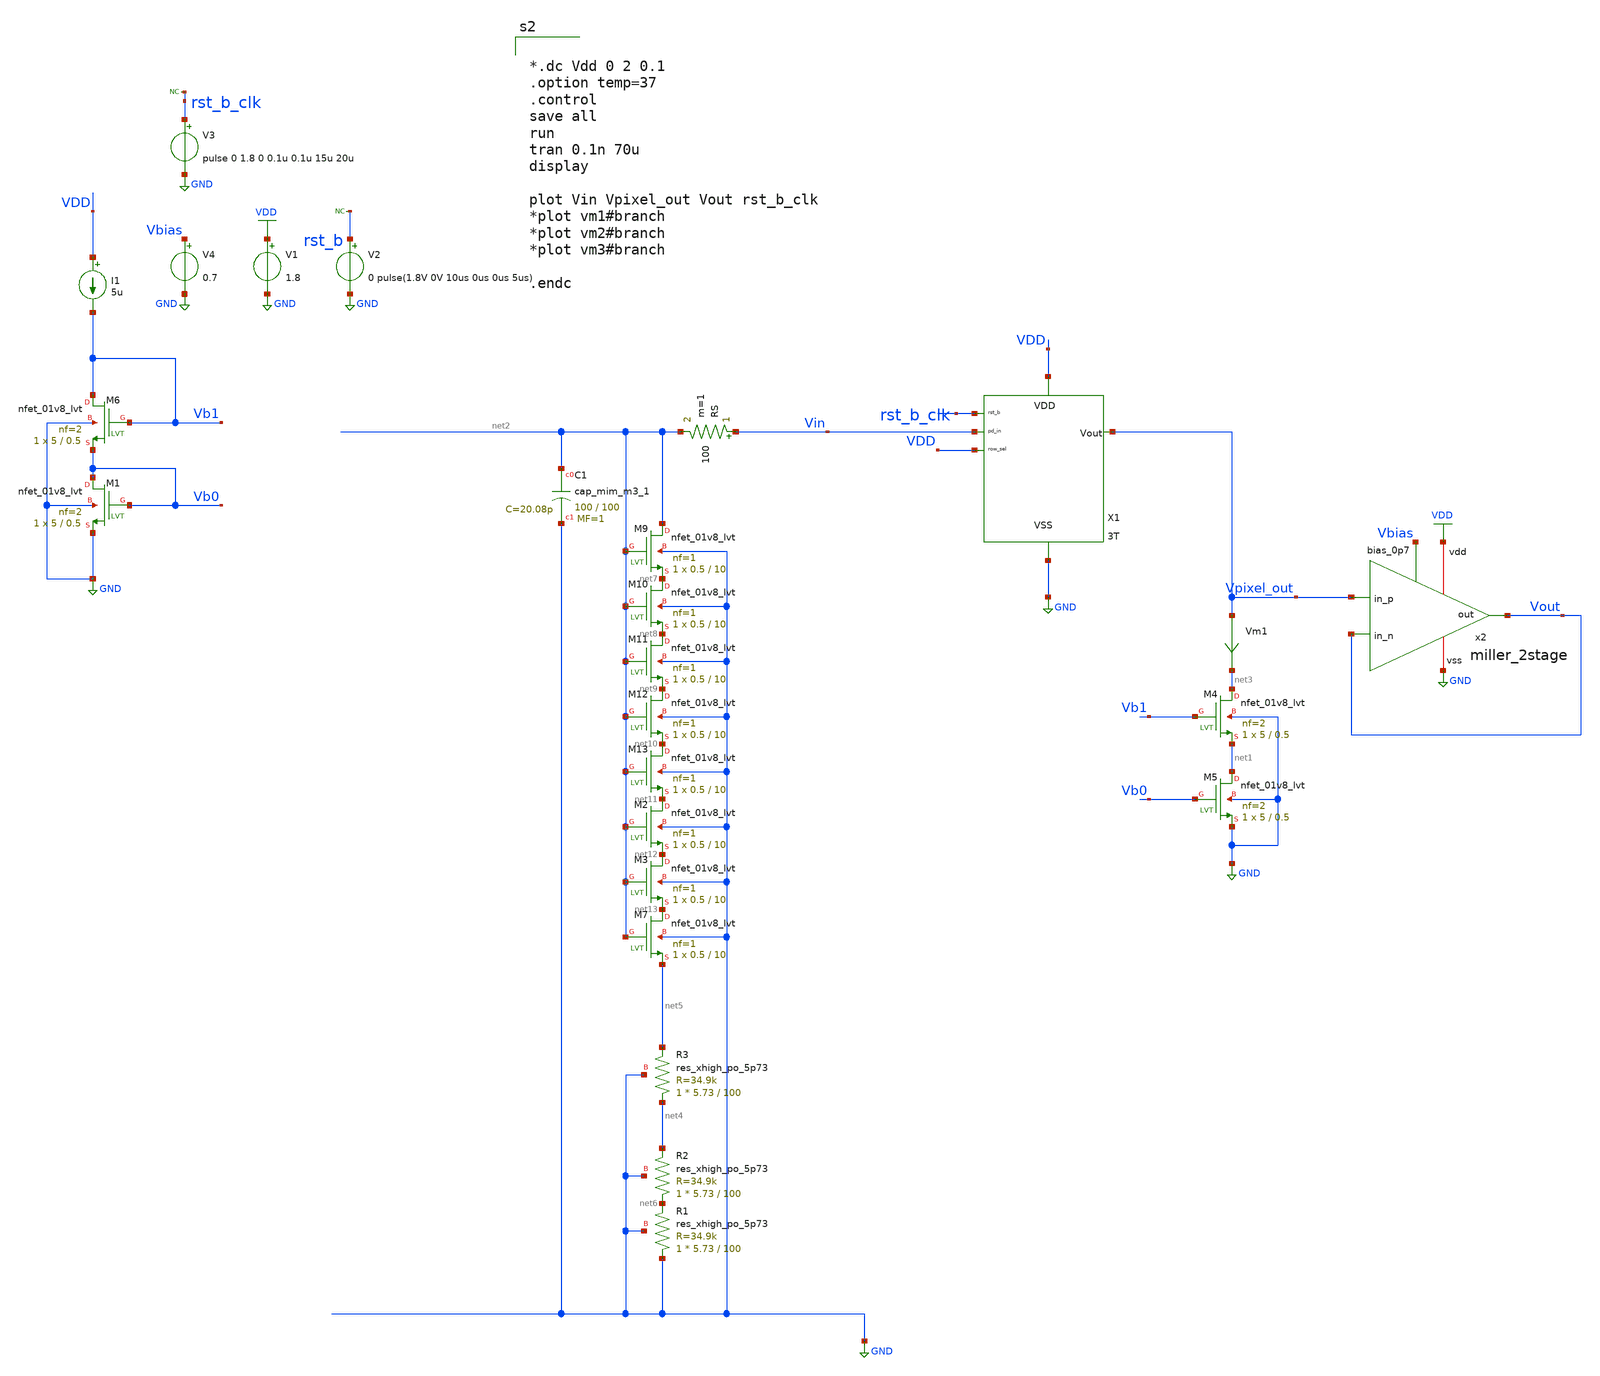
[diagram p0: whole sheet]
** sch_path: xschem/cmos_imager/tb_pixel_real_rc_buffer.sch
**.subckt tb_pixel_real_rc_buffer
XM4 net3 Vb1 net1 GND sky130_fd_pr__nfet_01v8_lvt L=0.5 W=5 nf=2 ad='int((nf+1)/2) * W/nf * 0.29' as='int((nf+2)/2) * W/nf * 0.29'
+ pd='2*int((nf+1)/2) * (W/nf + 0.29)' ps='2*int((nf+2)/2) * (W/nf + 0.29)' nrd='0.29 / W' nrs='0.29 / W'
+ sa=0 sb=0 sd=0 mult=1 m=1
XM5 net1 Vb0 GND GND sky130_fd_pr__nfet_01v8_lvt L=0.5 W=5 nf=2 ad='int((nf+1)/2) * W/nf * 0.29' as='int((nf+2)/2) * W/nf * 0.29'
+ pd='2*int((nf+1)/2) * (W/nf + 0.29)' ps='2*int((nf+2)/2) * (W/nf + 0.29)' nrd='0.29 / W' nrs='0.29 / W'
+ sa=0 sb=0 sd=0 mult=1 m=1
RS Vin net2 100 m=1
XM6 Vb1 Vb1 Vb0 GND sky130_fd_pr__nfet_01v8_lvt L=0.5 W=5 nf=2 ad='int((nf+1)/2) * W/nf * 0.29' as='int((nf+2)/2) * W/nf * 0.29'
+ pd='2*int((nf+1)/2) * (W/nf + 0.29)' ps='2*int((nf+2)/2) * (W/nf + 0.29)' nrd='0.29 / W' nrs='0.29 / W'
+ sa=0 sb=0 sd=0 mult=1 m=1
XM1 Vb0 Vb0 GND GND sky130_fd_pr__nfet_01v8_lvt L=0.5 W=5 nf=2 ad='int((nf+1)/2) * W/nf * 0.29' as='int((nf+2)/2) * W/nf * 0.29'
+ pd='2*int((nf+1)/2) * (W/nf + 0.29)' ps='2*int((nf+2)/2) * (W/nf + 0.29)' nrd='0.29 / W' nrs='0.29 / W'
+ sa=0 sb=0 sd=0 mult=1 m=1
I1 VDD Vb1 5u
V1 VDD GND 1.8
Vm1 Vpixel_out net3 0
.save i(vm1)
V2 rst_b GND 0 pulse(1.8V 0V 10us 0us 0us 5us)
X1 VDD Vin rst_b_clk VDD GND Vpixel_out 3T
XC1 net2 GND sky130_fd_pr__cap_mim_m3_1 W=100 L=100 MF=1 m=1
XR1 GND net6 GND sky130_fd_pr__res_xhigh_po_5p73 L=100 mult=1 m=1
XR2 net6 net4 GND sky130_fd_pr__res_xhigh_po_5p73 L=100 mult=1 m=1
XM9 net2 net2 net7 GND sky130_fd_pr__nfet_01v8_lvt L=10 W=0.5 nf=1 ad='int((nf+1)/2) * W/nf * 0.29' as='int((nf+2)/2) * W/nf * 0.29'
+ pd='2*int((nf+1)/2) * (W/nf + 0.29)' ps='2*int((nf+2)/2) * (W/nf + 0.29)' nrd='0.29 / W' nrs='0.29 / W'
+ sa=0 sb=0 sd=0 mult=1 m=1
XM10 net7 net2 net8 GND sky130_fd_pr__nfet_01v8_lvt L=10 W=0.5 nf=1 ad='int((nf+1)/2) * W/nf * 0.29'
+ as='int((nf+2)/2) * W/nf * 0.29' pd='2*int((nf+1)/2) * (W/nf + 0.29)' ps='2*int((nf+2)/2) * (W/nf + 0.29)'
+ nrd='0.29 / W' nrs='0.29 / W' sa=0 sb=0 sd=0 mult=1 m=1
XM11 net8 net2 net9 GND sky130_fd_pr__nfet_01v8_lvt L=10 W=0.5 nf=1 ad='int((nf+1)/2) * W/nf * 0.29'
+ as='int((nf+2)/2) * W/nf * 0.29' pd='2*int((nf+1)/2) * (W/nf + 0.29)' ps='2*int((nf+2)/2) * (W/nf + 0.29)'
+ nrd='0.29 / W' nrs='0.29 / W' sa=0 sb=0 sd=0 mult=1 m=1
XM12 net9 net2 net10 GND sky130_fd_pr__nfet_01v8_lvt L=10 W=0.5 nf=1 ad='int((nf+1)/2) * W/nf * 0.29'
+ as='int((nf+2)/2) * W/nf * 0.29' pd='2*int((nf+1)/2) * (W/nf + 0.29)' ps='2*int((nf+2)/2) * (W/nf + 0.29)'
+ nrd='0.29 / W' nrs='0.29 / W' sa=0 sb=0 sd=0 mult=1 m=1
XM13 net10 net2 net11 GND sky130_fd_pr__nfet_01v8_lvt L=10 W=0.5 nf=1 ad='int((nf+1)/2) * W/nf * 0.29'
+ as='int((nf+2)/2) * W/nf * 0.29' pd='2*int((nf+1)/2) * (W/nf + 0.29)' ps='2*int((nf+2)/2) * (W/nf + 0.29)'
+ nrd='0.29 / W' nrs='0.29 / W' sa=0 sb=0 sd=0 mult=1 m=1
XM2 net11 net2 net12 GND sky130_fd_pr__nfet_01v8_lvt L=10 W=0.5 nf=1 ad='int((nf+1)/2) * W/nf * 0.29'
+ as='int((nf+2)/2) * W/nf * 0.29' pd='2*int((nf+1)/2) * (W/nf + 0.29)' ps='2*int((nf+2)/2) * (W/nf + 0.29)'
+ nrd='0.29 / W' nrs='0.29 / W' sa=0 sb=0 sd=0 mult=1 m=1
XM3 net12 net2 net13 GND sky130_fd_pr__nfet_01v8_lvt L=10 W=0.5 nf=1 ad='int((nf+1)/2) * W/nf * 0.29'
+ as='int((nf+2)/2) * W/nf * 0.29' pd='2*int((nf+1)/2) * (W/nf + 0.29)' ps='2*int((nf+2)/2) * (W/nf + 0.29)'
+ nrd='0.29 / W' nrs='0.29 / W' sa=0 sb=0 sd=0 mult=1 m=1
XM7 net13 net2 net5 GND sky130_fd_pr__nfet_01v8_lvt L=10 W=0.5 nf=1 ad='int((nf+1)/2) * W/nf * 0.29'
+ as='int((nf+2)/2) * W/nf * 0.29' pd='2*int((nf+1)/2) * (W/nf + 0.29)' ps='2*int((nf+2)/2) * (W/nf + 0.29)'
+ nrd='0.29 / W' nrs='0.29 / W' sa=0 sb=0 sd=0 mult=1 m=1
V3 rst_b_clk GND pulse 0 1.8 0 0.1u 0.1u 15u 20u
* noconn rst_b_clk
* noconn rst_b
XR3 net4 net5 GND sky130_fd_pr__res_xhigh_po_5p73 L=100 mult=1 m=1
x2 VDD Vout Vpixel_out Vout Vbias GND miller_2stage
V4 Vbias GND 0.7
**** begin user architecture code

** opencircuitdesign pdks install
.lib $::SKYWATER_MODELS/sky130.lib.spice tt




*.dc Vdd 0 2 0.1
.option temp=37
.control
save all
run
tran 0.1n 70u
display

plot Vin Vpixel_out Vout rst_b_clk
*plot vm1#branch
*plot vm2#branch
*plot vm3#branch

.endc


**** end user architecture code
**.ends
.GLOBAL GND
.GLOBAL VDD
.end
